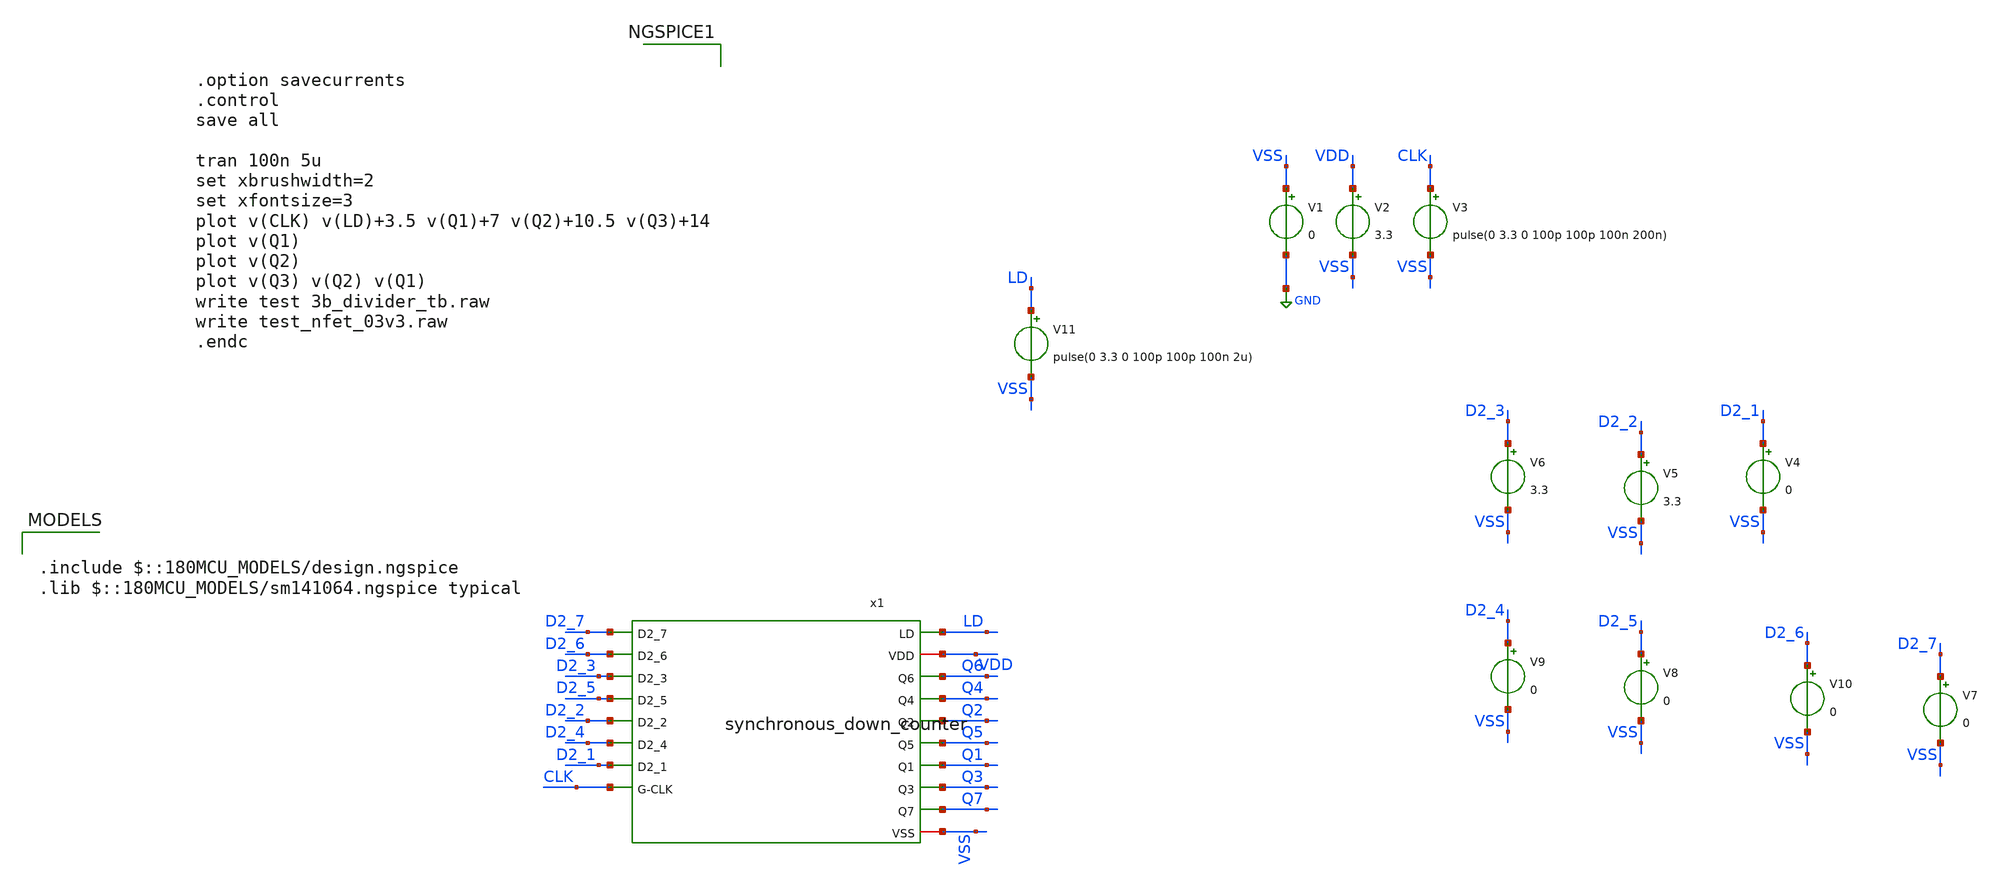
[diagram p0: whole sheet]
** sch_path: Clock_Generator_PAKISTAN_06/Xschem/untitled-20.sch
**.subckt untitled-20
V1 VSS GND 0
V2 VDD VSS 3.3
V3 CLK VSS pulse(0 3.3 0 100p 100p 100n 200n)
V4 D2_1 VSS 0
V5 D2_2 VSS 3.3
V6 D2_3 VSS 3.3
V8 D2_5 VSS 0
V9 D2_4 VSS 0
V7 D2_7 VSS 0
V10 D2_6 VSS 0
x1 LD VDD Q6 Q4 Q2 Q5 Q1 Q3 Q7 D2_7 D2_6 D2_3 D2_5 D2_2 D2_4 D2_1 CLK VSS synchronous_down_counter
V11 LD VSS pulse(0 3.3 0 100p 100p 100n 2u)
**** begin user architecture code


.option savecurrents
.control
save all

tran 100n 5u
set xbrushwidth=2
set xfontsize=3
plot v(CLK) v(LD)+3.5 v(Q1)+7 v(Q2)+10.5 v(Q3)+14
plot v(Q1)
plot v(Q2)
plot v(Q3) v(Q2) v(Q1)
write test 3b_divider_tb.raw
write test_nfet_03v3.raw
.endc



.include $::180MCU_MODELS/design.ngspice
.lib $::180MCU_MODELS/sm141064.ngspice typical

**** end user architecture code
**.ends
.GLOBAL GND
.end
